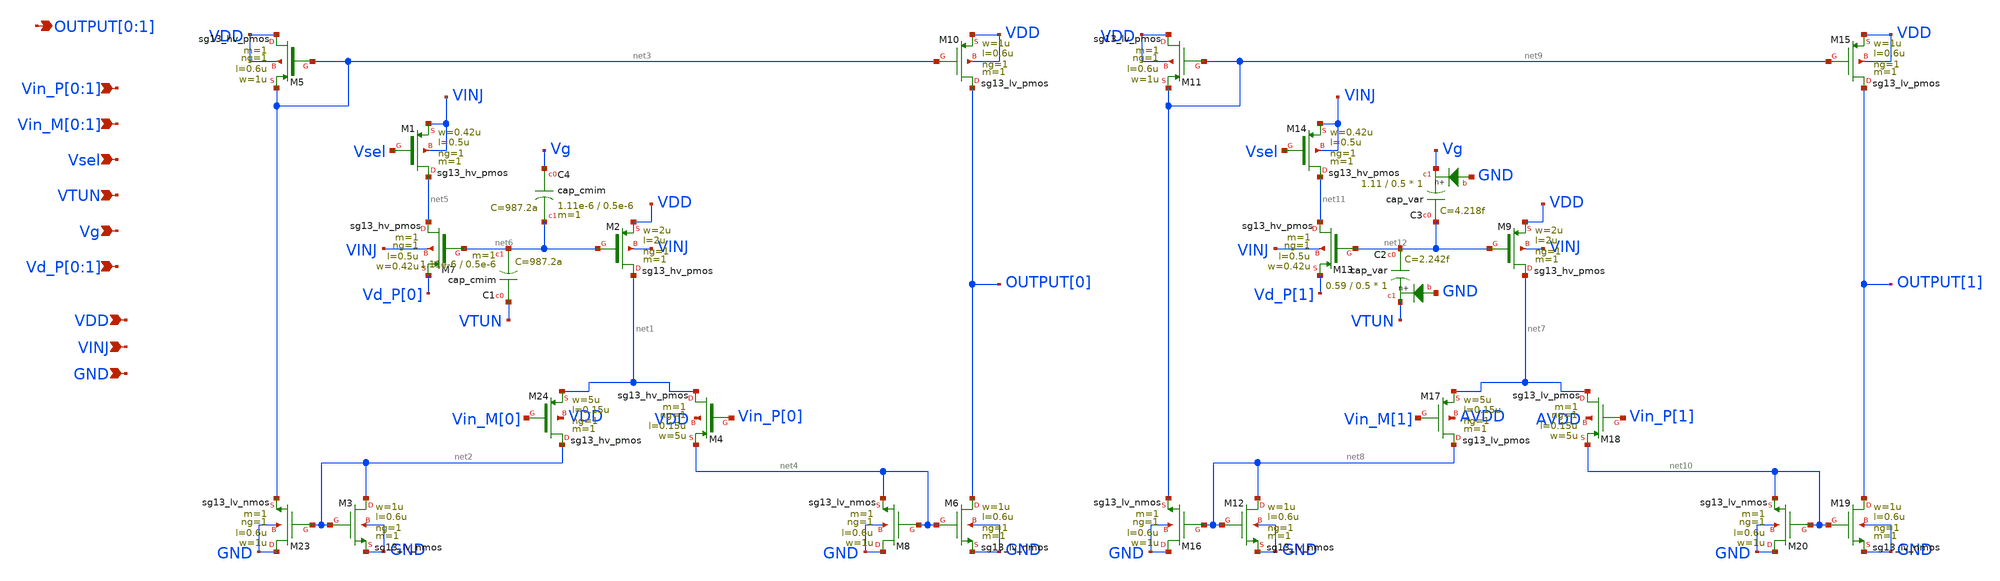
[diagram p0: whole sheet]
** sch_path: ihp130_cells/TA_FGBias_1x2/TA_FGbias_1x2.sch
**.subckt TA_FGbias_1x2 Vin_P[0],Vin_P[1] Vin_M[0],Vin_M[1] Vsel VTUN Vg VINJ OUTPUT[0],OUTPUT[1]
*+ VDD GND Vd_P[0],Vd_P[1]
*.ipin Vin_P[0],Vin_P[1]
*.ipin Vin_M[0],Vin_M[1]
*.ipin Vsel
*.ipin VTUN
*.ipin Vg
*.ipin VINJ
*.opin OUTPUT[0],OUTPUT[1]
*.ipin VDD
*.ipin GND
*.ipin Vd_P[0],Vd_P[1]
XC2 net12 VTUN GND sky130_fd_pr__cap_var W=0.59 L=0.5 VM=1 m=1
XC3 net12 Vg GND sky130_fd_pr__cap_var W=1.11 L=0.5 VM=1 m=1
XM23 GND net2 net3 GND sg13_lv_nmos w=1u l=0.6u ng=1 m=1 mm_ok=1
XM3 net2 net2 GND GND sg13_lv_nmos w=1u l=0.6u ng=1 m=1 mm_ok=1
XM4 net1 Vin_P[0] net4 VDD sg13_hv_pmos w=5u l=0.15u ng=1 m=1 mm_ok=1
XM24 net2 Vin_M[0] net1 VDD sg13_hv_pmos w=5u l=0.15u ng=1 m=1 mm_ok=1
XM5 VDD net3 net3 VDD sg13_hv_pmos w=1u l=0.6u ng=1 m=1 mm_ok=1
XM1 net5 Vsel VINJ VINJ sg13_hv_pmos w=0.42u l=0.5u ng=1 m=1 mm_ok=1
XM2 net1 net6 VDD VINJ sg13_hv_pmos w=2u l=2u ng=1 m=1 mm_ok=1
XM7 net5 net6 Vd_P[0] VINJ sg13_hv_pmos w=0.42u l=0.5u ng=1 m=1 mm_ok=1
XM6 OUTPUT[0] net4 GND GND sg13_lv_nmos w=1u l=0.6u ng=1 m=1 mm_ok=1
XM8 GND net4 net4 GND sg13_lv_nmos w=1u l=0.6u ng=1 m=1 mm_ok=1
XM10 OUTPUT[0] net3 VDD VDD sg13_lv_pmos w=1u l=0.6u ng=1 m=1 mm_ok=1
XM11 VDD net9 net9 VDD sg13_lv_pmos w=1u l=0.6u ng=1 m=1 mm_ok=1
XM12 net8 net8 GND GND sg13_lv_nmos w=1u l=0.6u ng=1 m=1 mm_ok=1
XM16 GND net8 net9 GND sg13_lv_nmos w=1u l=0.6u ng=1 m=1 mm_ok=1
XM19 OUTPUT[1] net10 GND GND sg13_lv_nmos w=1u l=0.6u ng=1 m=1 mm_ok=1
XM20 GND net10 net10 GND sg13_lv_nmos w=1u l=0.6u ng=1 m=1 mm_ok=1
XM15 OUTPUT[1] net9 VDD VDD sg13_lv_pmos w=1u l=0.6u ng=1 m=1 mm_ok=1
XM17 net8 Vin_M[1] net7 AVDD sg13_lv_pmos w=5u l=0.15u ng=1 m=1 mm_ok=1
XM18 net7 Vin_P[1] net10 AVDD sg13_lv_pmos w=5u l=0.15u ng=1 m=1 mm_ok=1
XM9 net7 net12 VDD VINJ sg13_hv_pmos w=2u l=2u ng=1 m=1 mm_ok=1
XM13 net11 net12 Vd_P[1] VINJ sg13_hv_pmos w=0.42u l=0.5u ng=1 m=1 mm_ok=1
XM14 net11 Vsel VINJ VINJ sg13_hv_pmos w=0.42u l=0.5u ng=1 m=1 mm_ok=1
XC4 Vg net6 cap_cmim w=1.11e-6 l=0.5e-6 m=1 mm_ok=1
XC1 VTUN net6 cap_cmim w=1.11e-6 l=0.5e-6 m=1 mm_ok=1
**.ends
.end
